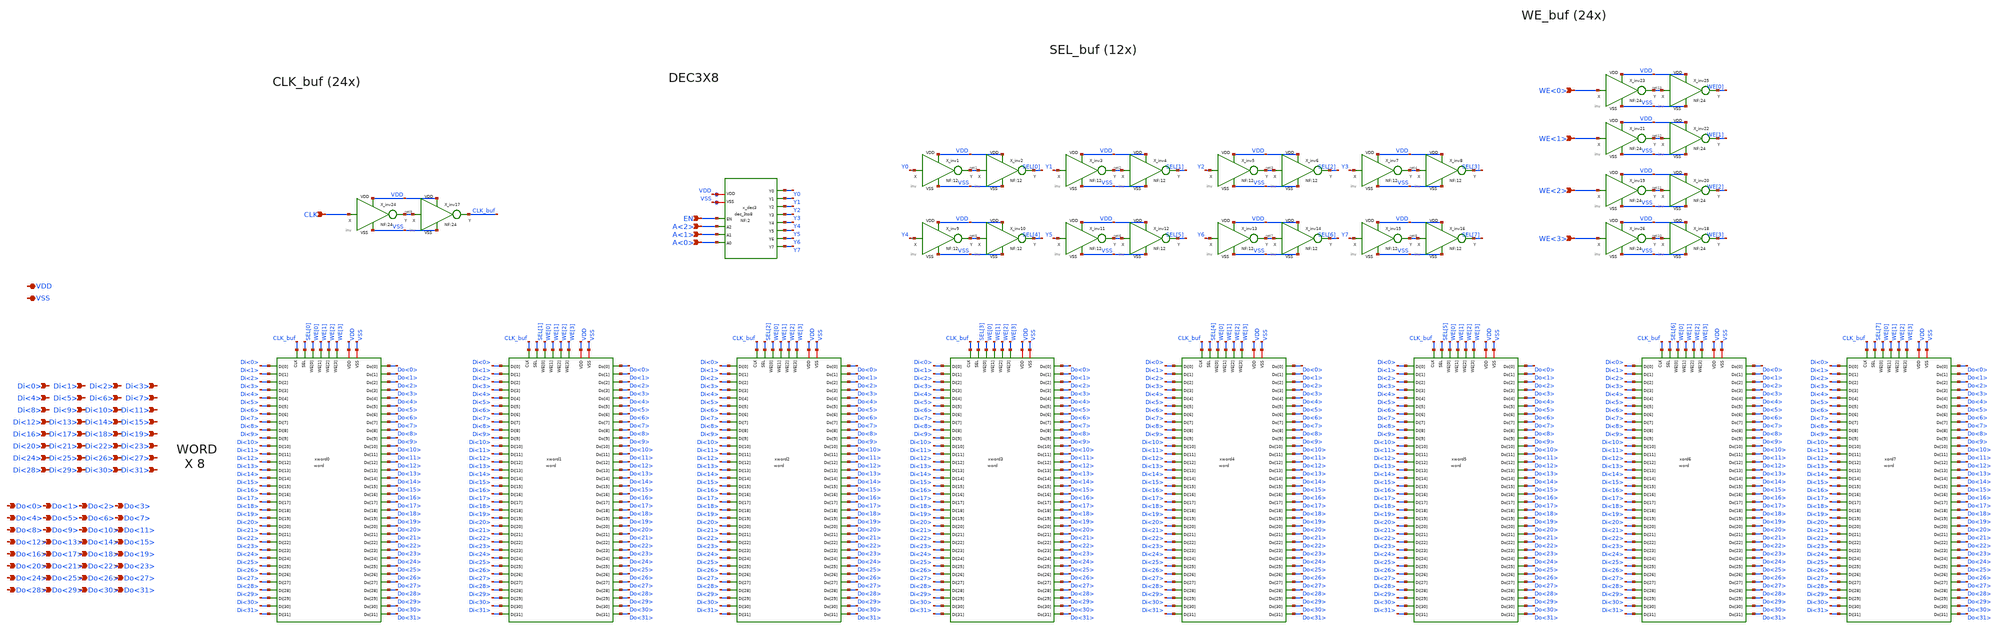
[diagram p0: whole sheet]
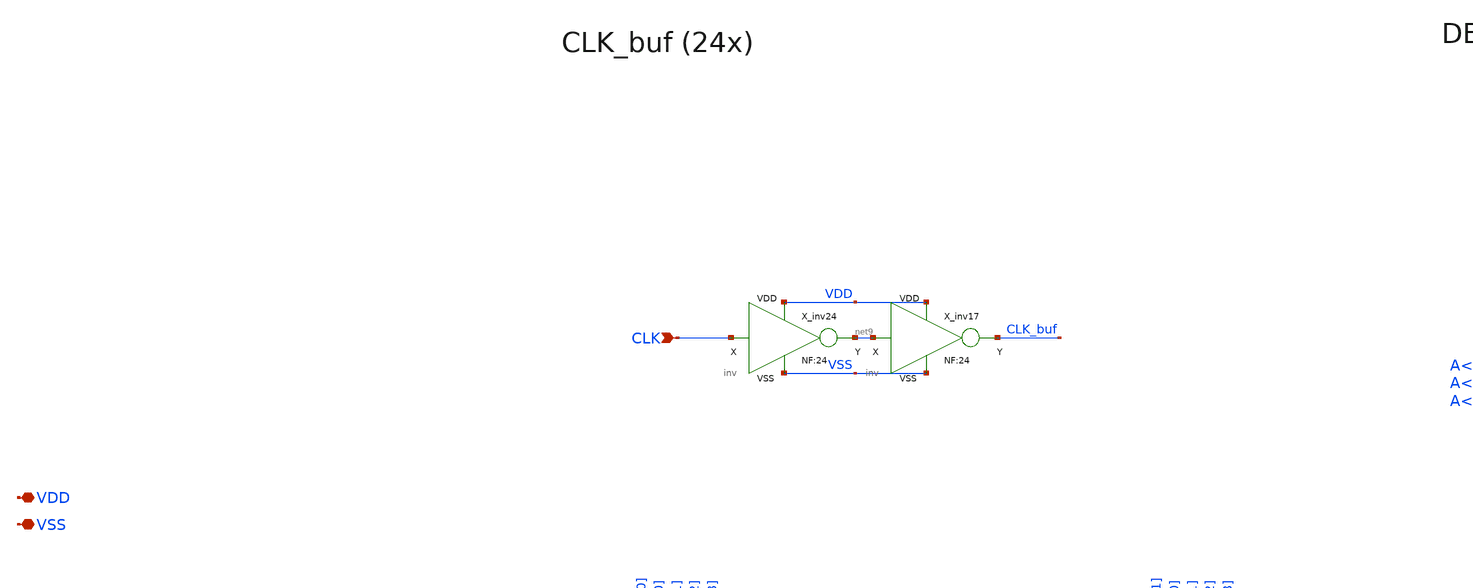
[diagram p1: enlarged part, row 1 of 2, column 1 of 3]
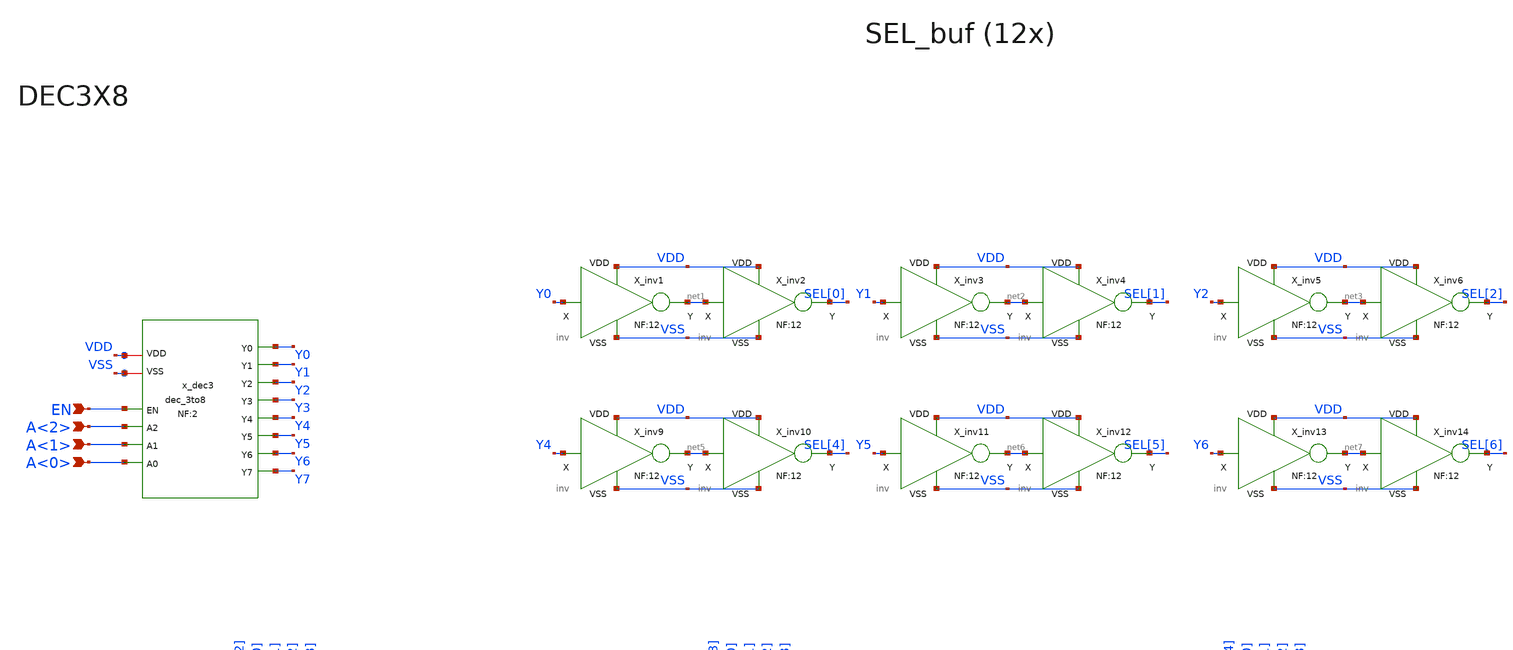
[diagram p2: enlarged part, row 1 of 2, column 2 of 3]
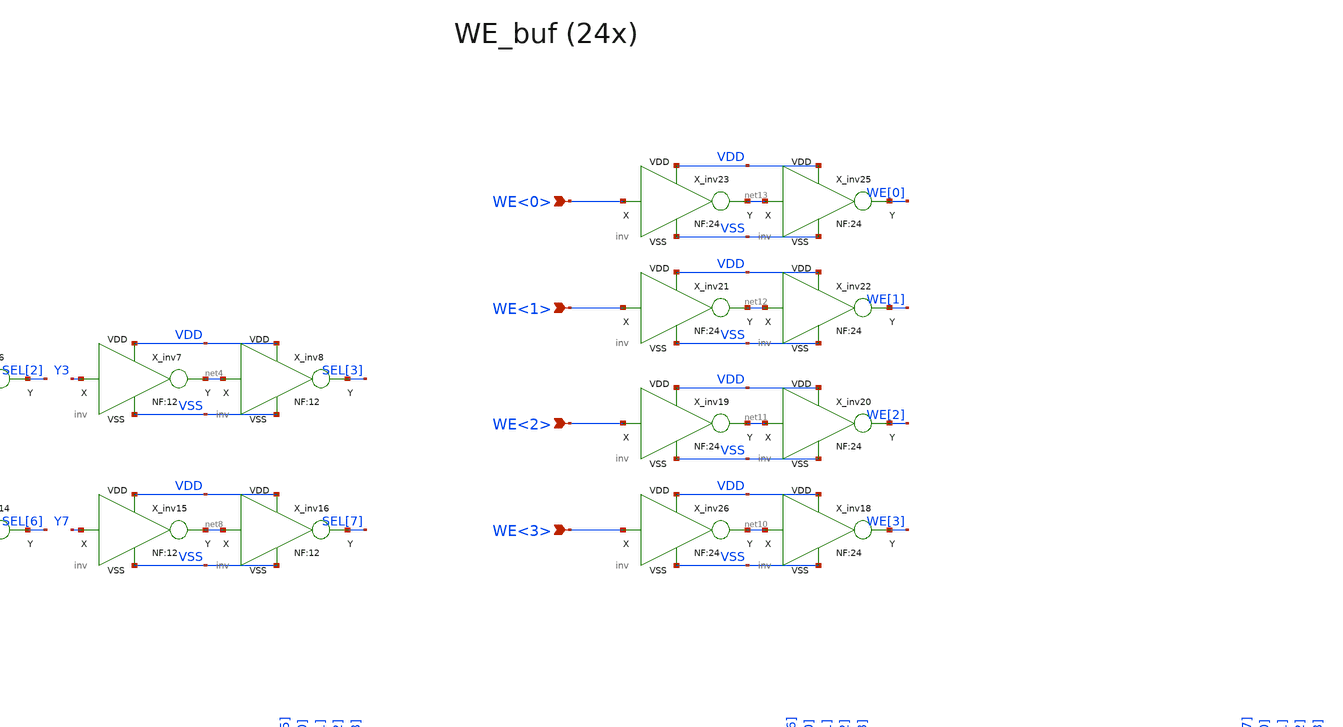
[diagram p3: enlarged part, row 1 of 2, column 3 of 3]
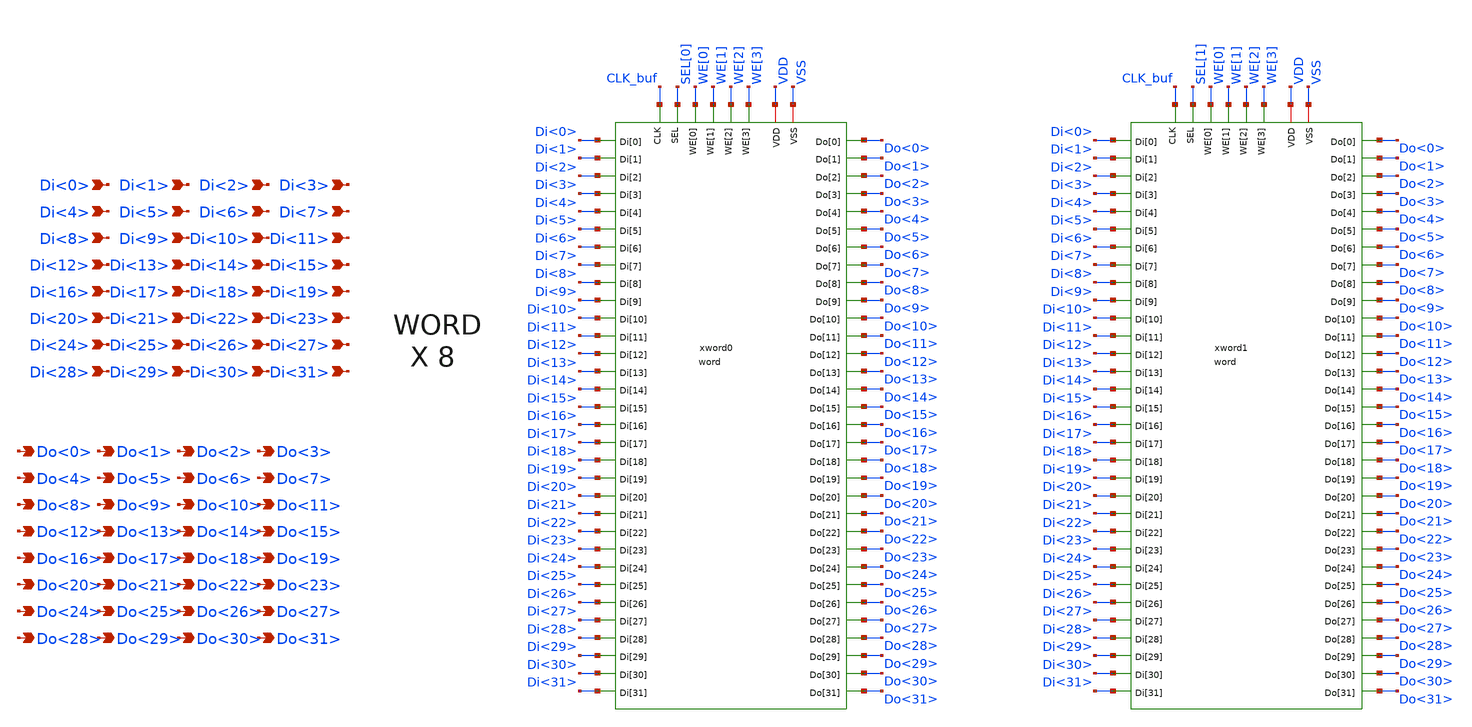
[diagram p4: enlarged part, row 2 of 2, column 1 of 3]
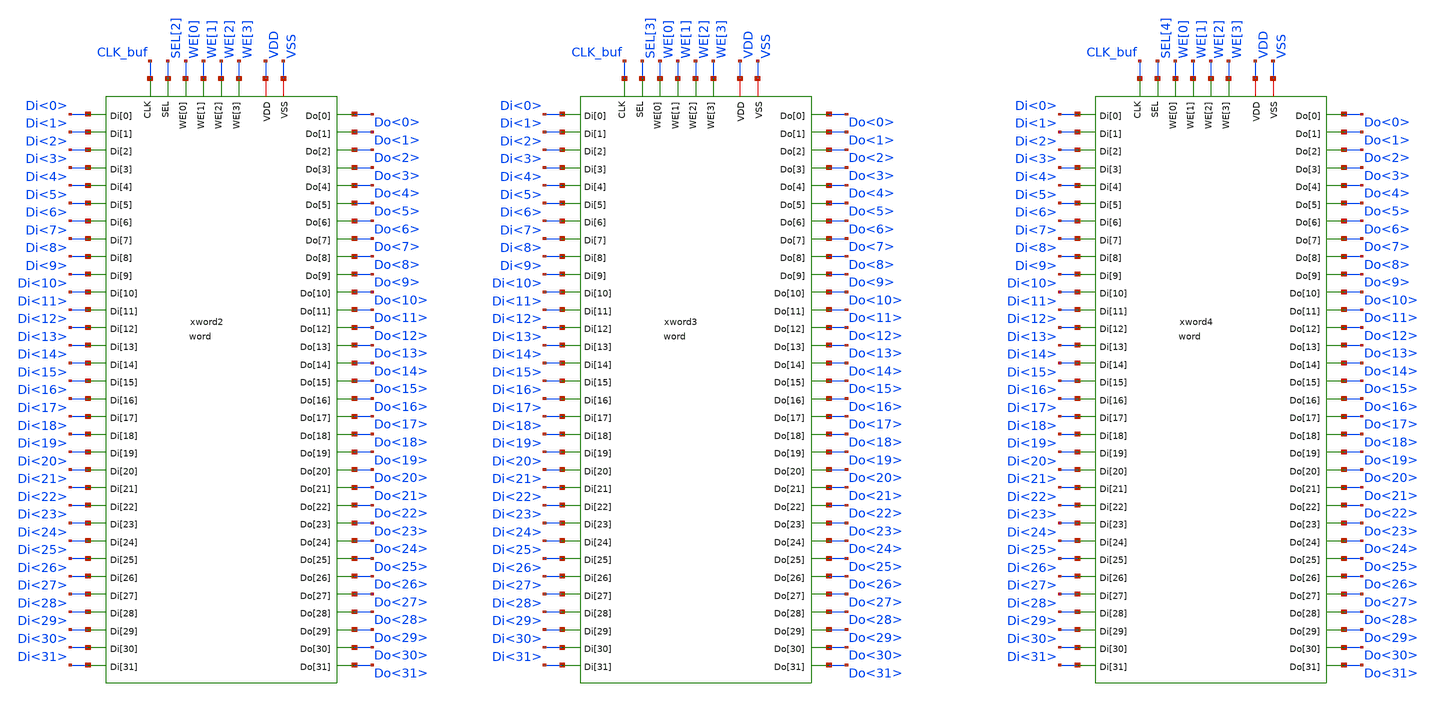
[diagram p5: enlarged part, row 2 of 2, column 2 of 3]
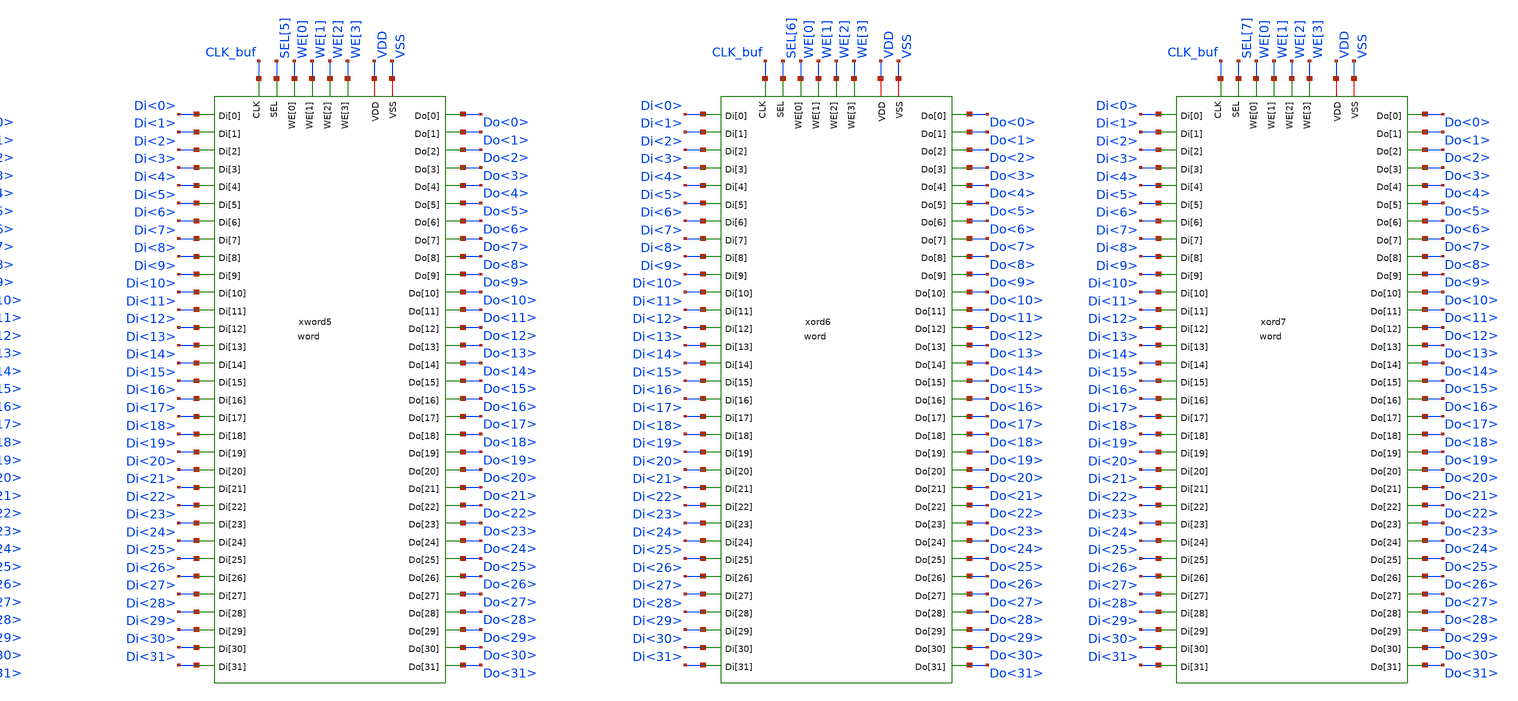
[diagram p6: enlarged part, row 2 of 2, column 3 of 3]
** sch_path: xschem_lib/sylee21/RAM8bit.sch
**.subckt RAM8bit EN A<2> A<1> A<0> Di<0> Di<1> Di<2> Di<3> Di<4> Di<5> Di<6> Di<7> Di<8> Di<9>
*+ Di<10> Di<11> Di<12> Di<13> Di<14> Di<15> Di<16> Di<17> Di<18> Di<19> Di<20> Di<21> Di<22> Di<23> Di<24>
*+ Di<25> Di<26> Di<27> Di<28> Di<29> Di<30> Di<31> VDD VSS WE<0> WE<1> WE<2> WE<3> CLK Do<0> Do<1> Do<2>
*+ Do<3> Do<4> Do<5> Do<6> Do<7> Do<8> Do<9> Do<10> Do<11> Do<12> Do<13> Do<14> Do<15> Do<16> Do<17> Do<18>
*+ Do<19> Do<20> Do<21> Do<22> Do<23> Do<24> Do<25> Do<26> Do<27> Do<28> Do<29> Do<30> Do<31>
*.ipin EN
*.ipin A<2>
*.ipin A<1>
*.ipin A<0>
*.ipin Di<0>
*.ipin Di<1>
*.ipin Di<2>
*.ipin Di<3>
*.ipin Di<4>
*.ipin Di<5>
*.ipin Di<6>
*.ipin Di<7>
*.ipin Di<8>
*.ipin Di<9>
*.ipin Di<10>
*.ipin Di<11>
*.ipin Di<12>
*.ipin Di<13>
*.ipin Di<14>
*.ipin Di<15>
*.ipin Di<16>
*.ipin Di<17>
*.ipin Di<18>
*.ipin Di<19>
*.ipin Di<20>
*.ipin Di<21>
*.ipin Di<22>
*.ipin Di<23>
*.ipin Di<24>
*.ipin Di<25>
*.ipin Di<26>
*.ipin Di<27>
*.ipin Di<28>
*.ipin Di<29>
*.ipin Di<30>
*.ipin Di<31>
*.iopin VDD
*.iopin VSS
*.ipin WE<0>
*.ipin WE<1>
*.ipin WE<2>
*.ipin WE<3>
*.ipin CLK
*.opin Do<0>
*.opin Do<1>
*.opin Do<2>
*.opin Do<3>
*.opin Do<4>
*.opin Do<5>
*.opin Do<6>
*.opin Do<7>
*.opin Do<8>
*.opin Do<9>
*.opin Do<10>
*.opin Do<11>
*.opin Do<12>
*.opin Do<13>
*.opin Do<14>
*.opin Do<15>
*.opin Do<16>
*.opin Do<17>
*.opin Do<18>
*.opin Do<19>
*.opin Do<20>
*.opin Do<21>
*.opin Do<22>
*.opin Do<23>
*.opin Do<24>
*.opin Do<25>
*.opin Do<26>
*.opin Do<27>
*.opin Do<28>
*.opin Do<29>
*.opin Do<30>
*.opin Do<31>
xword0 VDD VSS WE[3] WE[2] WE[1] WE[0] SEL[0] CLK_buf Di<9> Di<7> Di<19> Di<20> Di<30> Di<8> Di<10>
+ Di<4> Di<12> Di<24> Di<5> Di<23> Di<29> Di<3> Di<14> Di<18> Di<28> Di<17> Di<16> Di<27> Di<21> Di<22>
+ Di<0> Di<1> Di<31> Di<26> Di<25> Di<15> Di<2> Di<13> Di<6> Di<11> Do<21> Do<22> Do<27> Do<23> Do<28>
+ Do<8> Do<9> Do<10> Do<11> Do<12> Do<29> Do<30> Do<13> Do<14> Do<15> Do<16> Do<24> Do<17> Do<1> Do<7>
+ Do<6> Do<5> Do<18> Do<0> Do<2> Do<3> Do<4> Do<19> Do<20> Do<25> Do<26> Do<31> word NF=2
x_dec3 A<1> EN A<2> A<0> VDD VSS Y0 Y1 Y2 Y3 Y4 Y5 Y6 Y7 dec_3to8 NF=2
X_inv1 Y0 VDD VSS net1 inv NF=12
X_inv2 net1 VDD VSS SEL[0] inv NF=12
X_inv3 Y1 VDD VSS net2 inv NF=12
X_inv4 net2 VDD VSS SEL[1] inv NF=12
X_inv5 Y2 VDD VSS net3 inv NF=12
X_inv6 net3 VDD VSS SEL[2] inv NF=12
X_inv7 Y3 VDD VSS net4 inv NF=12
X_inv8 net4 VDD VSS SEL[3] inv NF=12
X_inv9 Y4 VDD VSS net5 inv NF=12
X_inv10 net5 VDD VSS SEL[4] inv NF=12
X_inv11 Y5 VDD VSS net6 inv NF=12
X_inv12 net6 VDD VSS SEL[5] inv NF=12
X_inv13 Y6 VDD VSS net7 inv NF=12
X_inv14 net7 VDD VSS SEL[6] inv NF=12
X_inv15 Y7 VDD VSS net8 inv NF=12
X_inv16 net8 VDD VSS SEL[7] inv NF=12
X_inv24 CLK VDD VSS net9 inv NF=24
X_inv17 net9 VDD VSS CLK_buf inv NF=24
X_inv26 WE<3> VDD VSS net10 inv NF=24
X_inv18 net10 VDD VSS WE[3] inv NF=24
X_inv19 WE<2> VDD VSS net11 inv NF=24
X_inv20 net11 VDD VSS WE[2] inv NF=24
X_inv21 WE<1> VDD VSS net12 inv NF=24
X_inv22 net12 VDD VSS WE[1] inv NF=24
X_inv23 WE<0> VDD VSS net13 inv NF=24
X_inv25 net13 VDD VSS WE[0] inv NF=24
xword1 VDD VSS WE[3] WE[2] WE[1] WE[0] SEL[1] CLK_buf Di<9> Di<7> Di<19> Di<20> Di<30> Di<8> Di<10>
+ Di<4> Di<12> Di<24> Di<5> Di<23> Di<29> Di<3> Di<14> Di<18> Di<28> Di<17> Di<16> Di<27> Di<21> Di<22>
+ Di<0> Di<1> Di<31> Di<26> Di<25> Di<15> Di<2> Di<13> Di<6> Di<11> Do<21> Do<22> Do<27> Do<23> Do<28>
+ Do<8> Do<9> Do<10> Do<11> Do<12> Do<29> Do<30> Do<13> Do<14> Do<15> Do<16> Do<24> Do<17> Do<1> Do<7>
+ Do<6> Do<5> Do<18> Do<0> Do<2> Do<3> Do<4> Do<19> Do<20> Do<25> Do<26> Do<31> word NF=2
xword2 VDD VSS WE[3] WE[2] WE[1] WE[0] SEL[2] CLK_buf Di<9> Di<7> Di<19> Di<20> Di<30> Di<8> Di<10>
+ Di<4> Di<12> Di<24> Di<5> Di<23> Di<29> Di<3> Di<14> Di<18> Di<28> Di<17> Di<16> Di<27> Di<21> Di<22>
+ Di<0> Di<1> Di<31> Di<26> Di<25> Di<15> Di<2> Di<13> Di<6> Di<11> Do<21> Do<22> Do<27> Do<23> Do<28>
+ Do<8> Do<9> Do<10> Do<11> Do<12> Do<29> Do<30> Do<13> Do<14> Do<15> Do<16> Do<24> Do<17> Do<1> Do<7>
+ Do<6> Do<5> Do<18> Do<0> Do<2> Do<3> Do<4> Do<19> Do<20> Do<25> Do<26> Do<31> word NF=2
xword3 VDD VSS WE[3] WE[2] WE[1] WE[0] SEL[3] CLK_buf Di<9> Di<7> Di<19> Di<20> Di<30> Di<8> Di<10>
+ Di<4> Di<12> Di<24> Di<5> Di<23> Di<29> Di<3> Di<14> Di<18> Di<28> Di<17> Di<16> Di<27> Di<21> Di<22>
+ Di<0> Di<1> Di<31> Di<26> Di<25> Di<15> Di<2> Di<13> Di<6> Di<11> Do<21> Do<22> Do<27> Do<23> Do<28>
+ Do<8> Do<9> Do<10> Do<11> Do<12> Do<29> Do<30> Do<13> Do<14> Do<15> Do<16> Do<24> Do<17> Do<1> Do<7>
+ Do<6> Do<5> Do<18> Do<0> Do<2> Do<3> Do<4> Do<19> Do<20> Do<25> Do<26> Do<31> word NF=2
xword4 VDD VSS WE[3] WE[2] WE[1] WE[0] SEL[4] CLK_buf Di<9> Di<7> Di<19> Di<20> Di<30> Di<8> Di<10>
+ Di<4> Di<12> Di<24> Di<5> Di<23> Di<29> Di<3> Di<14> Di<18> Di<28> Di<17> Di<16> Di<27> Di<21> Di<22>
+ Di<0> Di<1> Di<31> Di<26> Di<25> Di<15> Di<2> Di<13> Di<6> Di<11> Do<21> Do<22> Do<27> Do<23> Do<28>
+ Do<8> Do<9> Do<10> Do<11> Do<12> Do<29> Do<30> Do<13> Do<14> Do<15> Do<16> Do<24> Do<17> Do<1> Do<7>
+ Do<6> Do<5> Do<18> Do<0> Do<2> Do<3> Do<4> Do<19> Do<20> Do<25> Do<26> Do<31> word NF=2
xword5 VDD VSS WE[3] WE[2] WE[1] WE[0] SEL[5] CLK_buf Di<9> Di<7> Di<19> Di<20> Di<30> Di<8> Di<10>
+ Di<4> Di<12> Di<24> Di<5> Di<23> Di<29> Di<3> Di<14> Di<18> Di<28> Di<17> Di<16> Di<27> Di<21> Di<22>
+ Di<0> Di<1> Di<31> Di<26> Di<25> Di<15> Di<2> Di<13> Di<6> Di<11> Do<21> Do<22> Do<27> Do<23> Do<28>
+ Do<8> Do<9> Do<10> Do<11> Do<12> Do<29> Do<30> Do<13> Do<14> Do<15> Do<16> Do<24> Do<17> Do<1> Do<7>
+ Do<6> Do<5> Do<18> Do<0> Do<2> Do<3> Do<4> Do<19> Do<20> Do<25> Do<26> Do<31> word NF=2
xord6 VDD VSS WE[3] WE[2] WE[1] WE[0] SEL[6] CLK_buf Di<9> Di<7> Di<19> Di<20> Di<30> Di<8> Di<10>
+ Di<4> Di<12> Di<24> Di<5> Di<23> Di<29> Di<3> Di<14> Di<18> Di<28> Di<17> Di<16> Di<27> Di<21> Di<22>
+ Di<0> Di<1> Di<31> Di<26> Di<25> Di<15> Di<2> Di<13> Di<6> Di<11> Do<21> Do<22> Do<27> Do<23> Do<28>
+ Do<8> Do<9> Do<10> Do<11> Do<12> Do<29> Do<30> Do<13> Do<14> Do<15> Do<16> Do<24> Do<17> Do<1> Do<7>
+ Do<6> Do<5> Do<18> Do<0> Do<2> Do<3> Do<4> Do<19> Do<20> Do<25> Do<26> Do<31> word NF=2
xord7 VDD VSS WE[3] WE[2] WE[1] WE[0] SEL[7] CLK_buf Di<9> Di<7> Di<19> Di<20> Di<30> Di<8> Di<10>
+ Di<4> Di<12> Di<24> Di<5> Di<23> Di<29> Di<3> Di<14> Di<18> Di<28> Di<17> Di<16> Di<27> Di<21> Di<22>
+ Di<0> Di<1> Di<31> Di<26> Di<25> Di<15> Di<2> Di<13> Di<6> Di<11> Do<21> Do<22> Do<27> Do<23> Do<28>
+ Do<8> Do<9> Do<10> Do<11> Do<12> Do<29> Do<30> Do<13> Do<14> Do<15> Do<16> Do<24> Do<17> Do<1> Do<7>
+ Do<6> Do<5> Do<18> Do<0> Do<2> Do<3> Do<4> Do<19> Do<20> Do<25> Do<26> Do<31> word NF=2
**.ends
.end
